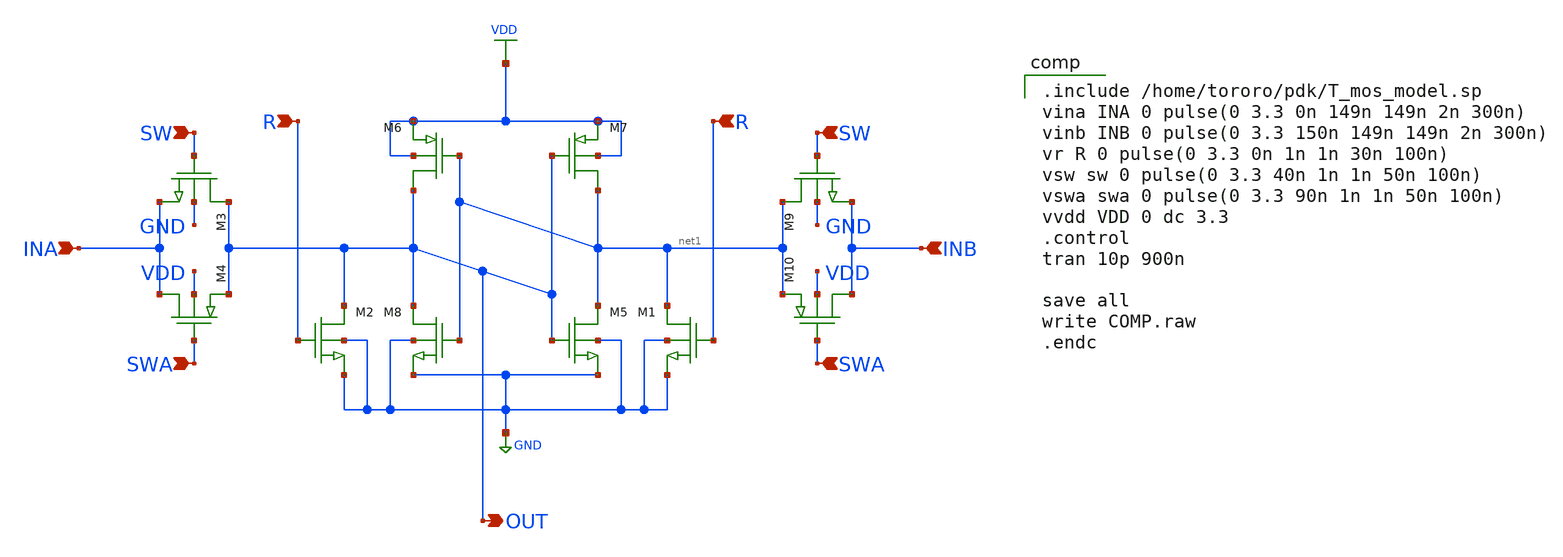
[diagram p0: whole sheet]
** sch_path: task_comp/COMP.sch
**.subckt COMP OUT INB INA R R SW SWA SW SWA
*.opin OUT
*.ipin INB
*.ipin INA
*.ipin R
*.ipin R
*.ipin SW
*.ipin SWA
*.ipin SW
*.ipin SWA
M5 net1 OUT GND GND nch w=9.7u l=1.94u as=0 ps=0 ad=0 pd=0 m=1
M6 OUT net1 VDD VDD pch w=9.7u l=0.35u as=0 ps=0 ad=0 pd=0 m=1
M7 net1 OUT VDD VDD pch w=9.7u l=0.35u as=0 ps=0 ad=0 pd=0 m=1
M8 OUT net1 GND GND nch w=9.7u l=1.94u as=0 ps=0 ad=0 pd=0 m=1
M1 net1 R GND GND nch w=9.7u l=1.94u as=0 ps=0 ad=0 pd=0 m=1
M2 OUT R GND GND nch w=9.7u l=1.94u as=0 ps=0 ad=0 pd=0 m=1
M3 OUT SW INA GND nch w=9.7u l=1.94u as=0 ps=0 ad=0 pd=0 m=1
M4 INA SWA OUT VDD pch w=9.7u l=0.35u as=0 ps=0 ad=0 pd=0 m=1
M9 net1 SW INB GND nch w=9.7u l=1.94u as=0 ps=0 ad=0 pd=0 m=1
M10 INB SWA net1 VDD pch w=9.7u l=0.35u as=0 ps=0 ad=0 pd=0 m=1
**** begin user architecture code

.include /home/tororo/pdk/T_mos_model.sp
vina INA 0 pulse(0 3.3 0n 149n 149n 2n 300n)
vinb INB 0 pulse(0 3.3 150n 149n 149n 2n 300n)
vr R 0 pulse(0 3.3 0n 1n 1n 30n 100n)
vsw sw 0 pulse(0 3.3 40n 1n 1n 50n 100n)
vswa swa 0 pulse(0 3.3 90n 1n 1n 50n 100n)
vvdd VDD 0 dc 3.3
.control
tran 10p 900n

save all
write COMP.raw
.endc

**** end user architecture code
**.ends
.GLOBAL VDD
.GLOBAL GND
.end
